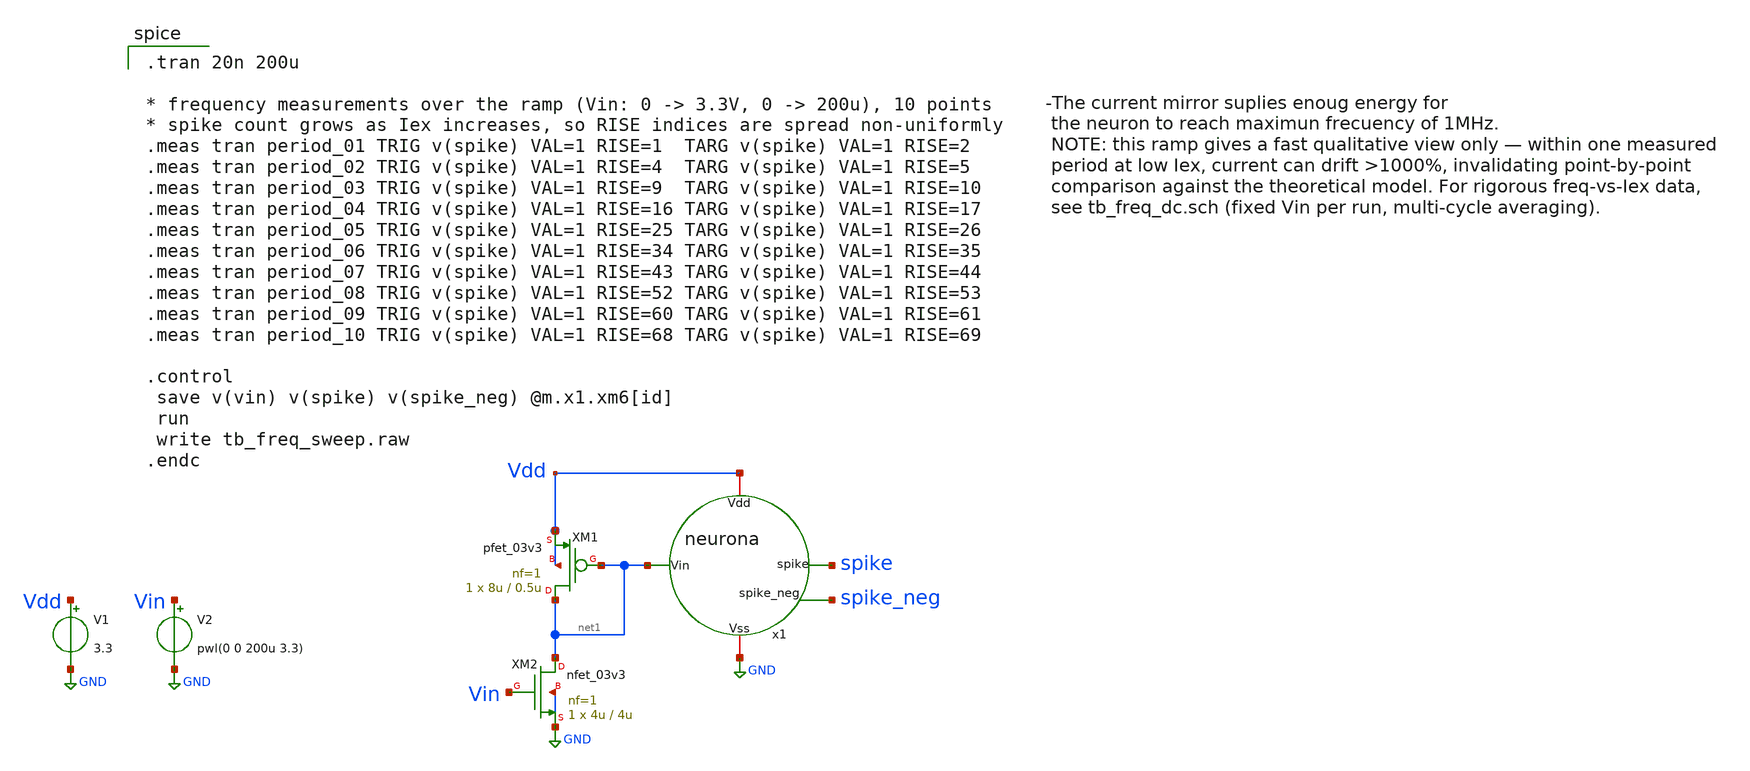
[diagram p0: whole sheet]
** sch_path: sch/lif/tb/tb_freq_sweep.sch
**.subckt tb_freq_sweep
V1 Vdd GND 3.3
V2 Vin GND pwl(0 0 200u 3.3)
XM1 net1 net1 Vdd Vdd pfet_03v3 L=0.5u W=8u nf=1 ad='int((nf+1)/2) * W/nf * 0.18u' as='int((nf+2)/2) * W/nf * 0.18u'
+ pd='2*int((nf+1)/2) * (W/nf + 0.18u)' ps='2*int((nf+2)/2) * (W/nf + 0.18u)' nrd='0.18u / W' nrs='0.18u / W'
+ sa=0 sb=0 sd=0 m=1
XM2 net1 Vin GND GND nfet_03v3 L=4u W=4u nf=1 ad='int((nf+1)/2) * W/nf * 0.18u' as='int((nf+2)/2) * W/nf * 0.18u'
+ pd='2*int((nf+1)/2) * (W/nf + 0.18u)' ps='2*int((nf+2)/2) * (W/nf + 0.18u)' nrd='0.18u / W' nrs='0.18u / W'
+ sa=0 sb=0 sd=0 m=1
x1 Vdd GND net1 spike spike_neg neurona
**** begin user architecture code

.tran 20n 200u

* frequency measurements over the ramp (Vin: 0 -> 3.3V, 0 -> 200u), 10 points
* spike count grows as Iex increases, so RISE indices are spread non-uniformly
.meas tran period_01 TRIG v(spike) VAL=1 RISE=1  TARG v(spike) VAL=1 RISE=2
.meas tran period_02 TRIG v(spike) VAL=1 RISE=4  TARG v(spike) VAL=1 RISE=5
.meas tran period_03 TRIG v(spike) VAL=1 RISE=9  TARG v(spike) VAL=1 RISE=10
.meas tran period_04 TRIG v(spike) VAL=1 RISE=16 TARG v(spike) VAL=1 RISE=17
.meas tran period_05 TRIG v(spike) VAL=1 RISE=25 TARG v(spike) VAL=1 RISE=26
.meas tran period_06 TRIG v(spike) VAL=1 RISE=34 TARG v(spike) VAL=1 RISE=35
.meas tran period_07 TRIG v(spike) VAL=1 RISE=43 TARG v(spike) VAL=1 RISE=44
.meas tran period_08 TRIG v(spike) VAL=1 RISE=52 TARG v(spike) VAL=1 RISE=53
.meas tran period_09 TRIG v(spike) VAL=1 RISE=60 TARG v(spike) VAL=1 RISE=61
.meas tran period_10 TRIG v(spike) VAL=1 RISE=68 TARG v(spike) VAL=1 RISE=69

.control
 save v(vin) v(spike) v(spike_neg) @m.x1.xm6[id]
 run
 write tb_freq_sweep.raw
.endc


.include $::180MCU_MODELS/design.ngspice
.lib $::180MCU_MODELS/sm141064.ngspice typical

**** end user architecture code
**.ends

* expanding   symbol:  /foss/designs/CapiMagics/sch/lif/neurona.sym # of pins=5
** sym_path: /foss/designs/CapiMagics/sch/lif/neurona.sym
** sch_path: /foss/designs/CapiMagics/sch/lif/neurona.sch
.subckt neurona Vdd Vss Vin spike spike_neg
*.iopin Vdd
*.iopin Vss
*.ipin Vin
*.opin spike
*.opin spike_neg
XM1 spike_neg integration Vdd Vdd pfet_03v3 L=0.28u W=0.22u nf=1 ad='int((nf+1)/2) * W/nf * 0.18u' as='int((nf+2)/2) * W/nf * 0.18u'
+ pd='2*int((nf+1)/2) * (W/nf + 0.18u)' ps='2*int((nf+2)/2) * (W/nf + 0.18u)' nrd='0.18u / W' nrs='0.18u / W'
+ sa=0 sb=0 sd=0 m=1
XM2 spike_neg integration Vss Vss nfet_03v3 L=0.28u W=0.22u nf=1 ad='int((nf+1)/2) * W/nf * 0.18u' as='int((nf+2)/2) * W/nf * 0.18u'
+ pd='2*int((nf+1)/2) * (W/nf + 0.18u)' ps='2*int((nf+2)/2) * (W/nf + 0.18u)' nrd='0.18u / W' nrs='0.18u / W'
+ sa=0 sb=0 sd=0 m=1
XM3 spike/reset spike_neg Vdd Vdd pfet_03v3 L=0.28u W=0.22u nf=1 ad='int((nf+1)/2) * W/nf * 0.18u' as='int((nf+2)/2) * W/nf * 0.18u'
+ pd='2*int((nf+1)/2) * (W/nf + 0.18u)' ps='2*int((nf+2)/2) * (W/nf + 0.18u)' nrd='0.18u / W' nrs='0.18u / W'
+ sa=0 sb=0 sd=0 m=1
XM4 spike/reset spike_neg Vss Vss nfet_03v3 L=0.28u W=0.22u nf=1 ad='int((nf+1)/2) * W/nf * 0.18u' as='int((nf+2)/2) * W/nf * 0.18u'
+ pd='2*int((nf+1)/2) * (W/nf + 0.18u)' ps='2*int((nf+2)/2) * (W/nf + 0.18u)' nrd='0.18u / W' nrs='0.18u / W'
+ sa=0 sb=0 sd=0 m=1
XM7 spike spike_neg Vdd Vdd pfet_03v3 L=0.28u W=0.22u nf=1 ad='int((nf+1)/2) * W/nf * 0.18u' as='int((nf+2)/2) * W/nf * 0.18u'
+ pd='2*int((nf+1)/2) * (W/nf + 0.18u)' ps='2*int((nf+2)/2) * (W/nf + 0.18u)' nrd='0.18u / W' nrs='0.18u / W'
+ sa=0 sb=0 sd=0 m=1
XM8 spike spike_neg GND GND nfet_03v3 L=0.28u W=0.22u nf=1 ad='int((nf+1)/2) * W/nf * 0.18u' as='int((nf+2)/2) * W/nf * 0.18u'
+ pd='2*int((nf+1)/2) * (W/nf + 0.18u)' ps='2*int((nf+2)/2) * (W/nf + 0.18u)' nrd='0.18u / W' nrs='0.18u / W'
+ sa=0 sb=0 sd=0 m=1
XM5 integration spike/reset Vss Vss nfet_03v3 L=50u W=1.25u nf=1 ad='int((nf+1)/2) * W/nf * 0.18u' as='int((nf+2)/2) * W/nf * 0.18u'
+ pd='2*int((nf+1)/2) * (W/nf + 0.18u)' ps='2*int((nf+2)/2) * (W/nf + 0.18u)' nrd='0.18u / W' nrs='0.18u / W'
+ sa=0 sb=0 sd=0 m=1
C1 integration Vss 150f m=1
XM6 integration Vin Vdd Vdd pfet_03v3 L=17u W=0.22u nf=1 ad='int((nf+1)/2) * W/nf * 0.18u' as='int((nf+2)/2) * W/nf * 0.18u'
+ pd='2*int((nf+1)/2) * (W/nf + 0.18u)' ps='2*int((nf+2)/2) * (W/nf + 0.18u)' nrd='0.18u / W' nrs='0.18u / W'
+ sa=0 sb=0 sd=0 m=1
.ends

.GLOBAL GND
.end
